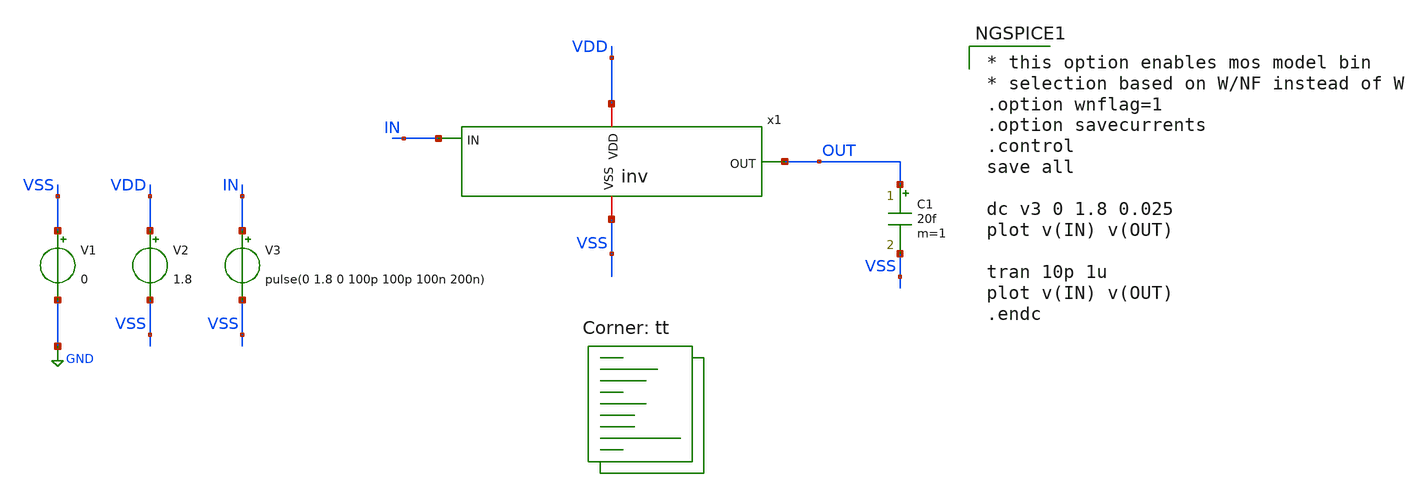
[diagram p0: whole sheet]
** sch_path: Xschem/inv_tb2.sch
* Copyright 2021 Stefan Frederik Schippers
* Licensed under the Apache License, Version 2.0 (the "License");
* you may not use this file except in compliance with the License.
* You may obtain a copy of the License at
* https://www.apache.org/licenses/LICENSE-2.0
* Unless required by applicable law or agreed to in writing, software
* distributed under the License is distributed on an "AS IS" BASIS,
* WITHOUT WARRANTIES OR CONDITIONS OF ANY KIND, either express or implied.
* See the License for the specific language governing permissions and
* limitations under the License.
**.subckt inv_tb2
x1 VSS VDD OUT IN inv
V1 VSS GND 0
V2 VDD VSS 1.8
V3 IN VSS pulse(0 1.8 0 100p 100p 100n 200n)
C1 OUT VSS 20f m=1
**** begin user architecture code
.lib $::SKYWATER_MODELS/sky130.lib.spice tt

* this option enables mos model bin
* selection based on W/NF instead of W
.option wnflag=1
.option savecurrents
.control
save all

dc v3 0 1.8 0.025
plot v(IN) v(OUT)

tran 10p 1u
plot v(IN) v(OUT)
.endc


**** end user architecture code
**.ends

* expanding   symbol:  inv.sym # of pins=4
** sym_path: Xschem/inv.sym
** sch_path: Xschem/inv.sch
.subckt inv VSS VDD OUT IN
*.iopin VDD
*.iopin VSS
*.ipin IN
*.opin OUT
XM1 OUT IN VSS VSS sky130_fd_pr__nfet_01v8 L=0.15 W=1 nf=1 ad='int((nf+1)/2) * W/nf * 0.29' as='int((nf+2)/2) * W/nf * 0.29'
+ pd='2*int((nf+1)/2) * (W/nf + 0.29)' ps='2*int((nf+2)/2) * (W/nf + 0.29)' nrd='0.29 / W' nrs='0.29 / W'
+ sa=0 sb=0 sd=0 mult=1 m=1
XM2 OUT IN VDD VDD sky130_fd_pr__pfet_01v8 L=0.15 W=3 nf=1 ad='int((nf+1)/2) * W/nf * 0.29' as='int((nf+2)/2) * W/nf * 0.29'
+ pd='2*int((nf+1)/2) * (W/nf + 0.29)' ps='2*int((nf+2)/2) * (W/nf + 0.29)' nrd='0.29 / W' nrs='0.29 / W'
+ sa=0 sb=0 sd=0 mult=1 m=1
.ends

.GLOBAL GND
.end
